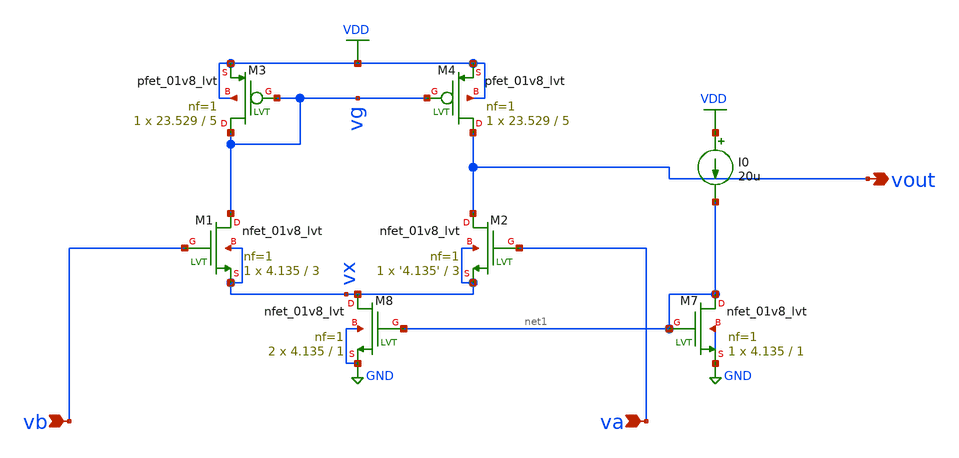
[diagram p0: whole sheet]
** sch_path: schematics/amplifier_with_bias_current-only-ckt.sch
**.subckt amplifier_with_bias_current-only-ckt vb va vout
*.ipin vb
*.ipin va
*.opin vout
XM4 vout vg VDD VDD sky130_fd_pr__pfet_01v8_lvt L=5 W=23.529 nf=1 ad='int((nf+1)/2) * W/nf * 0.29' as='int((nf+2)/2) * W/nf * 0.29'
+ pd='2*int((nf+1)/2) * (W/nf + 0.29)' ps='2*int((nf+2)/2) * (W/nf + 0.29)' nrd='0.29 / W' nrs='0.29 / W'
+ sa=0 sb=0 sd=0 mult=1 m=1
XM2 vout va vx vx sky130_fd_pr__nfet_01v8_lvt L=3 W='4.135' nf=1 ad='int((nf+1)/2) * W/nf * 0.29' as='int((nf+2)/2) * W/nf * 0.29'
+ pd='2*int((nf+1)/2) * (W/nf + 0.29)' ps='2*int((nf+2)/2) * (W/nf + 0.29)' nrd='0.29 / W' nrs='0.29 / W'
+ sa=0 sb=0 sd=0 mult=1 m=1
XM1 vg vb vx vx sky130_fd_pr__nfet_01v8_lvt L=3 W=4.135 nf=1 ad='int((nf+1)/2) * W/nf * 0.29' as='int((nf+2)/2) * W/nf * 0.29'
+ pd='2*int((nf+1)/2) * (W/nf + 0.29)' ps='2*int((nf+2)/2) * (W/nf + 0.29)' nrd='0.29 / W' nrs='0.29 / W'
+ sa=0 sb=0 sd=0 mult=1 m=1
XM7 net1 net1 GND GND sky130_fd_pr__nfet_01v8_lvt L=1 W=4.135 nf=1 ad='int((nf+1)/2) * W/nf * 0.29' as='int((nf+2)/2) * W/nf * 0.29'
+ pd='2*int((nf+1)/2) * (W/nf + 0.29)' ps='2*int((nf+2)/2) * (W/nf + 0.29)' nrd='0.29 / W' nrs='0.29 / W'
+ sa=0 sb=0 sd=0 mult=1 m=1
XM3 vg vg VDD VDD sky130_fd_pr__pfet_01v8_lvt L=5 W=23.529 nf=1 ad='int((nf+1)/2) * W/nf * 0.29' as='int((nf+2)/2) * W/nf * 0.29'
+ pd='2*int((nf+1)/2) * (W/nf + 0.29)' ps='2*int((nf+2)/2) * (W/nf + 0.29)' nrd='0.29 / W' nrs='0.29 / W'
+ sa=0 sb=0 sd=0 mult=1 m=1
XM8 vx net1 GND GND sky130_fd_pr__nfet_01v8_lvt L=1 W=4.135 nf=1 ad='int((nf+1)/2) * W/nf * 0.29' as='int((nf+2)/2) * W/nf * 0.29'
+ pd='2*int((nf+1)/2) * (W/nf + 0.29)' ps='2*int((nf+2)/2) * (W/nf + 0.29)' nrd='0.29 / W' nrs='0.29 / W'
+ sa=0 sb=0 sd=0 mult=2 m=2
I0 VDD net1 20u
**.ends
.GLOBAL GND
.GLOBAL VDD
.end
